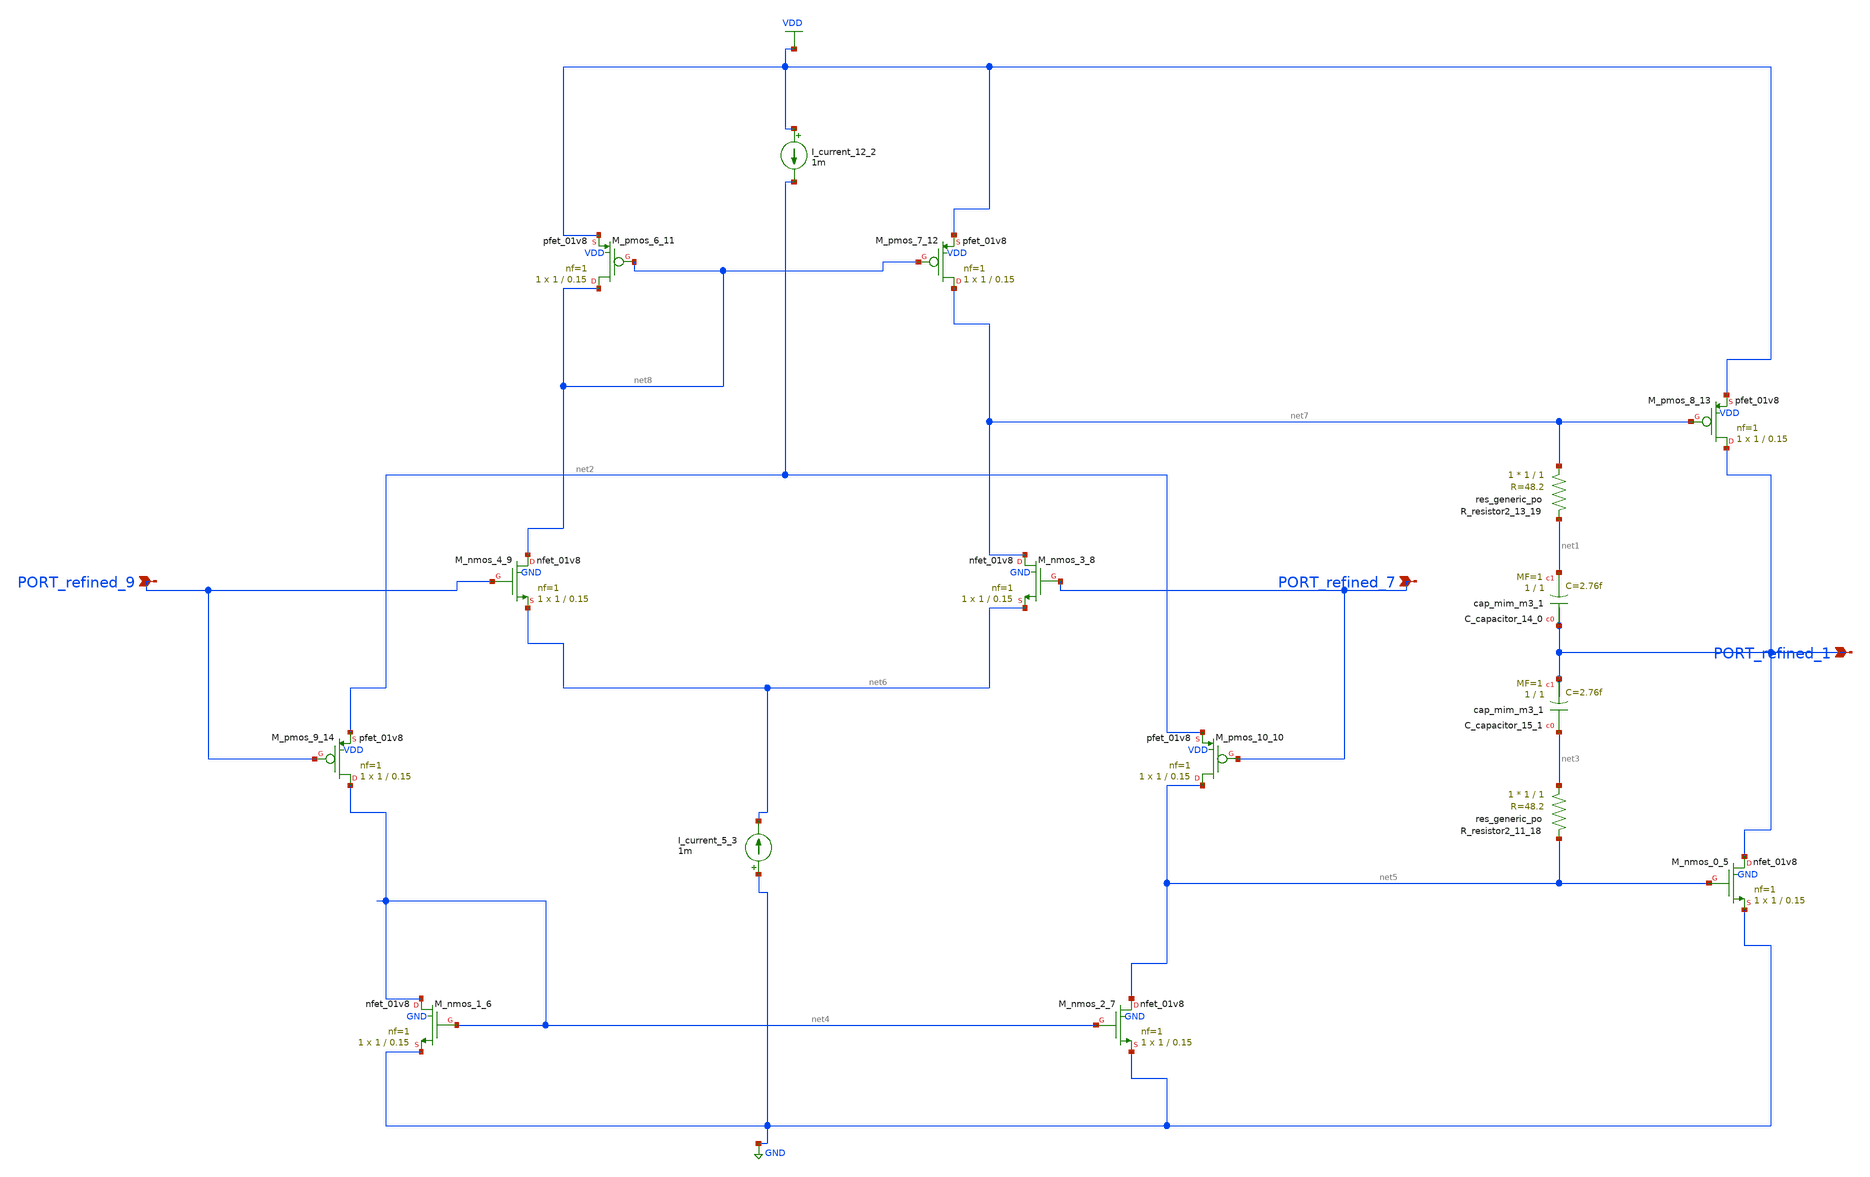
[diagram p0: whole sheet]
** sch_path: schematics/SchemGen/10_14445_23488549_IJECE-V10I12P102_06_001.sch
**.subckt 10_14445_23488549_IJECE-V10I12P102_06_001 PORT_refined_1 PORT_refined_7 PORT_refined_9
*.ipin PORT_refined_1
*.ipin PORT_refined_7
*.ipin PORT_refined_9
XC_capacitor_14_0 PORT_refined_1 net1 sky130_fd_pr__cap_mim_m3_1 W=1 L=1 MF=1 m=1
XC_capacitor_15_1 net3 PORT_refined_1 sky130_fd_pr__cap_mim_m3_1 W=1 L=1 MF=1 m=1
I_current_12_2 VDD net2 1m
I_current_5_3 GND net6 1m
XM_nmos_0_5 PORT_refined_1 net5 GND GND sky130_fd_pr__nfet_01v8 L=0.15 W=1 nf=1 ad='int((1 + 1)/2) * 1 / 1 * 0.29'
+ as='int((1 + 2)/2) * 1 / 1 * 0.29' pd='2*int((1 + 1)/2) * (1 / 1 + 0.29)' ps='2*int((1 + 2)/2) * (1 / 1 + 0.29)'
+ nrd='0.29 / 1 ' nrs='0.29 / 1 ' sa=0 sb=0 sd=0 mult=1 m=1
XM_nmos_1_6 net4 net4 GND GND sky130_fd_pr__nfet_01v8 L=0.15 W=1 nf=1 ad='int((1 + 1)/2) * 1 / 1 * 0.29'
+ as='int((1 + 2)/2) * 1 / 1 * 0.29' pd='2*int((1 + 1)/2) * (1 / 1 + 0.29)' ps='2*int((1 + 2)/2) * (1 / 1 + 0.29)'
+ nrd='0.29 / 1 ' nrs='0.29 / 1 ' sa=0 sb=0 sd=0 mult=1 m=1
XM_nmos_2_7 net5 net4 GND GND sky130_fd_pr__nfet_01v8 L=0.15 W=1 nf=1 ad='int((1 + 1)/2) * 1 / 1 * 0.29'
+ as='int((1 + 2)/2) * 1 / 1 * 0.29' pd='2*int((1 + 1)/2) * (1 / 1 + 0.29)' ps='2*int((1 + 2)/2) * (1 / 1 + 0.29)'
+ nrd='0.29 / 1 ' nrs='0.29 / 1 ' sa=0 sb=0 sd=0 mult=1 m=1
XM_nmos_3_8 net7 PORT_refined_7 net6 GND sky130_fd_pr__nfet_01v8 L=0.15 W=1 nf=1 ad='int((1 + 1)/2) * 1 / 1 * 0.29'
+ as='int((1 + 2)/2) * 1 / 1 * 0.29' pd='2*int((1 + 1)/2) * (1 / 1 + 0.29)' ps='2*int((1 + 2)/2) * (1 / 1 + 0.29)'
+ nrd='0.29 / 1 ' nrs='0.29 / 1 ' sa=0 sb=0 sd=0 mult=1 m=1
XM_nmos_4_9 net8 PORT_refined_9 net6 GND sky130_fd_pr__nfet_01v8 L=0.15 W=1 nf=1 ad='int((1 + 1)/2) * 1 / 1 * 0.29'
+ as='int((1 + 2)/2) * 1 / 1 * 0.29' pd='2*int((1 + 1)/2) * (1 / 1 + 0.29)' ps='2*int((1 + 2)/2) * (1 / 1 + 0.29)'
+ nrd='0.29 / 1 ' nrs='0.29 / 1 ' sa=0 sb=0 sd=0 mult=1 m=1
XM_pmos_10_10 net5 PORT_refined_7 net2 VDD sky130_fd_pr__pfet_01v8 L=0.15 W=1 nf=1 ad='int((1 + 1)/2) * 1 / 1 * 0.29'
+ as='int((1 + 2)/2) * 1 / 1 * 0.29' pd='2*int((1 + 1)/2) * (1 / 1 + 0.29)' ps='2*int((1 + 2)/2) * (1 / 1 + 0.29)'
+ nrd='0.29 / 1 ' nrs='0.29 / 1 ' sa=0 sb=0 sd=0 mult=1 m=1
XM_pmos_6_11 net8 net8 VDD VDD sky130_fd_pr__pfet_01v8 L=0.15 W=1 nf=1 ad='int((1 + 1)/2) * 1 / 1 * 0.29'
+ as='int((1 + 2)/2) * 1 / 1 * 0.29' pd='2*int((1 + 1)/2) * (1 / 1 + 0.29)' ps='2*int((1 + 2)/2) * (1 / 1 + 0.29)'
+ nrd='0.29 / 1 ' nrs='0.29 / 1 ' sa=0 sb=0 sd=0 mult=1 m=1
XM_pmos_7_12 net7 net8 VDD VDD sky130_fd_pr__pfet_01v8 L=0.15 W=1 nf=1 ad='int((1 + 1)/2) * 1 / 1 * 0.29'
+ as='int((1 + 2)/2) * 1 / 1 * 0.29' pd='2*int((1 + 1)/2) * (1 / 1 + 0.29)' ps='2*int((1 + 2)/2) * (1 / 1 + 0.29)'
+ nrd='0.29 / 1 ' nrs='0.29 / 1 ' sa=0 sb=0 sd=0 mult=1 m=1
XM_pmos_8_13 PORT_refined_1 net7 VDD VDD sky130_fd_pr__pfet_01v8 L=0.15 W=1 nf=1 ad='int((1 + 1)/2) * 1 / 1 * 0.29'
+ as='int((1 + 2)/2) * 1 / 1 * 0.29' pd='2*int((1 + 1)/2) * (1 / 1 + 0.29)' ps='2*int((1 + 2)/2) * (1 / 1 + 0.29)'
+ nrd='0.29 / 1 ' nrs='0.29 / 1 ' sa=0 sb=0 sd=0 mult=1 m=1
XM_pmos_9_14 net4 PORT_refined_9 net2 VDD sky130_fd_pr__pfet_01v8 L=0.15 W=1 nf=1 ad='int((1 + 1)/2) * 1 / 1 * 0.29'
+ as='int((1 + 2)/2) * 1 / 1 * 0.29' pd='2*int((1 + 1)/2) * (1 / 1 + 0.29)' ps='2*int((1 + 2)/2) * (1 / 1 + 0.29)'
+ nrd='0.29 / 1 ' nrs='0.29 / 1 ' sa=0 sb=0 sd=0 mult=1 m=1
XR_resistor2_11_18 net3 net5 sky130_fd_pr__res_generic_po W=1 L=1 m=1
XR_resistor2_13_19 net7 net1 sky130_fd_pr__res_generic_po W=1 L=1 m=1
**.ends
.GLOBAL GND
.GLOBAL VDD
.end
